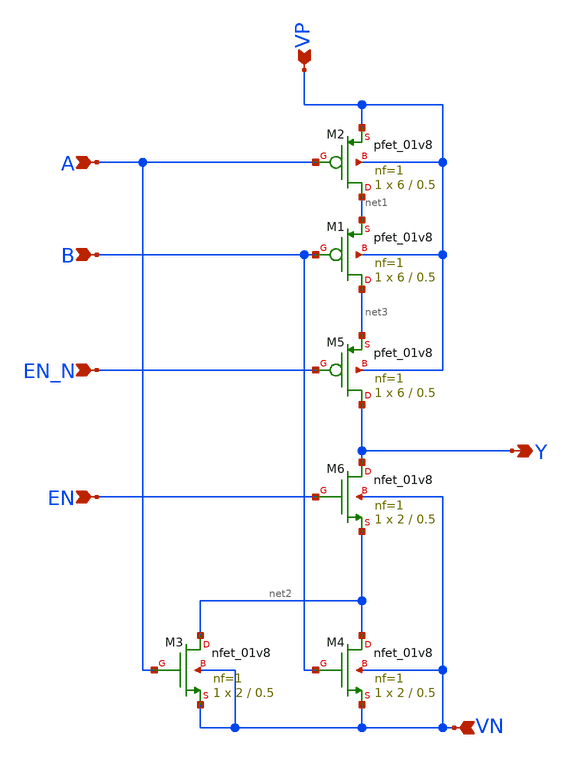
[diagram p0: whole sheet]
** sch_path: ADC/16bit_C2C/MagicAndSpice/EE431_FinalProj/tristate_NOR2.sch
**.subckt tristate_NOR2 A B VP VN Y EN_N EN
*.ipin A
*.ipin B
*.ipin VP
*.ipin VN
*.opin Y
*.ipin EN_N
*.ipin EN
XM1 net3 B net1 VP sky130_fd_pr__pfet_01v8 L=0.5 W=6 nf=1 ad='int((nf+1)/2) * W/nf * 0.29' as='int((nf+2)/2) * W/nf * 0.29'
+ pd='2*int((nf+1)/2) * (W/nf + 0.29)' ps='2*int((nf+2)/2) * (W/nf + 0.29)' nrd='0.29 / W' nrs='0.29 / W'
+ sa=0 sb=0 sd=0 mult=1 m=1
XM2 net1 A VP VP sky130_fd_pr__pfet_01v8 L=0.5 W=6 nf=1 ad='int((nf+1)/2) * W/nf * 0.29' as='int((nf+2)/2) * W/nf * 0.29'
+ pd='2*int((nf+1)/2) * (W/nf + 0.29)' ps='2*int((nf+2)/2) * (W/nf + 0.29)' nrd='0.29 / W' nrs='0.29 / W'
+ sa=0 sb=0 sd=0 mult=1 m=1
XM3 net2 A VN VN sky130_fd_pr__nfet_01v8 L=0.5 W=2 nf=1 ad='int((nf+1)/2) * W/nf * 0.29' as='int((nf+2)/2) * W/nf * 0.29'
+ pd='2*int((nf+1)/2) * (W/nf + 0.29)' ps='2*int((nf+2)/2) * (W/nf + 0.29)' nrd='0.29 / W' nrs='0.29 / W'
+ sa=0 sb=0 sd=0 mult=1 m=1
XM4 net2 B VN VN sky130_fd_pr__nfet_01v8 L=0.5 W=2 nf=1 ad='int((nf+1)/2) * W/nf * 0.29' as='int((nf+2)/2) * W/nf * 0.29'
+ pd='2*int((nf+1)/2) * (W/nf + 0.29)' ps='2*int((nf+2)/2) * (W/nf + 0.29)' nrd='0.29 / W' nrs='0.29 / W'
+ sa=0 sb=0 sd=0 mult=1 m=1
XM5 Y EN_N net3 VP sky130_fd_pr__pfet_01v8 L=0.5 W=6 nf=1 ad='int((nf+1)/2) * W/nf * 0.29' as='int((nf+2)/2) * W/nf * 0.29'
+ pd='2*int((nf+1)/2) * (W/nf + 0.29)' ps='2*int((nf+2)/2) * (W/nf + 0.29)' nrd='0.29 / W' nrs='0.29 / W'
+ sa=0 sb=0 sd=0 mult=1 m=1
XM6 Y EN net2 VN sky130_fd_pr__nfet_01v8 L=0.5 W=2 nf=1 ad='int((nf+1)/2) * W/nf * 0.29' as='int((nf+2)/2) * W/nf * 0.29'
+ pd='2*int((nf+1)/2) * (W/nf + 0.29)' ps='2*int((nf+2)/2) * (W/nf + 0.29)' nrd='0.29 / W' nrs='0.29 / W'
+ sa=0 sb=0 sd=0 mult=1 m=1
**.ends
.end
